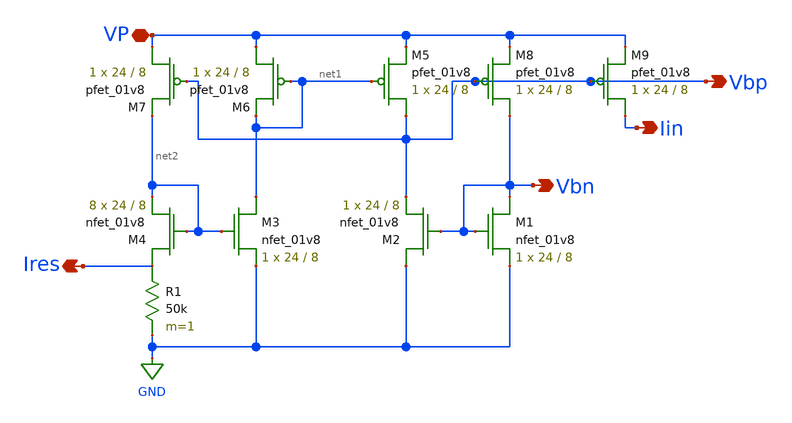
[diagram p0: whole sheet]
** sch_path: xschem/old_files/biasGen-j.sch
**.subckt biasGen-j Iin Vbp Vbn VP Ires
*.opin Iin
*.opin Vbp
*.opin Vbn
*.iopin VP
*.opin Ires
XM1 Vbn Vbn GND GND sky130_fd_pr__nfet_01v8 L=8 W=24 nf=1 ad='int((nf+1)/2) * W/nf * 0.29' as='int((nf+2)/2) * W/nf * 0.29'
+ pd='2*int((nf+1)/2) * (W/nf + 0.29)' ps='2*int((nf+2)/2) * (W/nf + 0.29)' nrd='0.29 / W' nrs='0.29 / W'
+ sa=0 sb=0 sd=0 mult=1 m=1
XM2 GND Vbn Vbp GND sky130_fd_pr__nfet_01v8 L=8 W=24 nf=1 ad='int((nf+1)/2) * W/nf * 0.29' as='int((nf+2)/2) * W/nf * 0.29'
+ pd='2*int((nf+1)/2) * (W/nf + 0.29)' ps='2*int((nf+2)/2) * (W/nf + 0.29)' nrd='0.29 / W' nrs='0.29 / W'
+ sa=0 sb=0 sd=0 mult=1 m=1
XM3 net1 net2 GND GND sky130_fd_pr__nfet_01v8 L=8 W=24 nf=1 ad='int((nf+1)/2) * W/nf * 0.29' as='int((nf+2)/2) * W/nf * 0.29'
+ pd='2*int((nf+1)/2) * (W/nf + 0.29)' ps='2*int((nf+2)/2) * (W/nf + 0.29)' nrd='0.29 / W' nrs='0.29 / W'
+ sa=0 sb=0 sd=0 mult=1 m=1
XM4 Ires net2 net2 GND sky130_fd_pr__nfet_01v8 L=8 W=24 nf=1 ad='int((nf+1)/2) * W/nf * 0.29' as='int((nf+2)/2) * W/nf * 0.29'
+ pd='2*int((nf+1)/2) * (W/nf + 0.29)' ps='2*int((nf+2)/2) * (W/nf + 0.29)' nrd='0.29 / W' nrs='0.29 / W'
+ sa=0 sb=0 sd=0 mult=8 m=8
XM5 Vbp net1 VP VDD sky130_fd_pr__pfet_01v8 L=8 W=24 nf=1 ad='int((nf+1)/2) * W/nf * 0.29' as='int((nf+2)/2) * W/nf * 0.29'
+ pd='2*int((nf+1)/2) * (W/nf + 0.29)' ps='2*int((nf+2)/2) * (W/nf + 0.29)' nrd='0.29 / W' nrs='0.29 / W'
+ sa=0 sb=0 sd=0 mult=1 m=1
XM6 VP net1 net1 VDD sky130_fd_pr__pfet_01v8 L=8 W=24 nf=1 ad='int((nf+1)/2) * W/nf * 0.29' as='int((nf+2)/2) * W/nf * 0.29'
+ pd='2*int((nf+1)/2) * (W/nf + 0.29)' ps='2*int((nf+2)/2) * (W/nf + 0.29)' nrd='0.29 / W' nrs='0.29 / W'
+ sa=0 sb=0 sd=0 mult=1 m=1
XM7 VP Vbp net2 VDD sky130_fd_pr__pfet_01v8 L=8 W=24 nf=1 ad='int((nf+1)/2) * W/nf * 0.29' as='int((nf+2)/2) * W/nf * 0.29'
+ pd='2*int((nf+1)/2) * (W/nf + 0.29)' ps='2*int((nf+2)/2) * (W/nf + 0.29)' nrd='0.29 / W' nrs='0.29 / W'
+ sa=0 sb=0 sd=0 mult=1 m=1
XM8 Vbn Vbp VP VDD sky130_fd_pr__pfet_01v8 L=8 W=24 nf=1 ad='int((nf+1)/2) * W/nf * 0.29' as='int((nf+2)/2) * W/nf * 0.29'
+ pd='2*int((nf+1)/2) * (W/nf + 0.29)' ps='2*int((nf+2)/2) * (W/nf + 0.29)' nrd='0.29 / W' nrs='0.29 / W'
+ sa=0 sb=0 sd=0 mult=1 m=1
R1 Ires GND 50k m=1
XM9 Iin Vbp VP VDD sky130_fd_pr__pfet_01v8 L=8 W=24 nf=1 ad='int((nf+1)/2) * W/nf * 0.29' as='int((nf+2)/2) * W/nf * 0.29'
+ pd='2*int((nf+1)/2) * (W/nf + 0.29)' ps='2*int((nf+2)/2) * (W/nf + 0.29)' nrd='0.29 / W' nrs='0.29 / W'
+ sa=0 sb=0 sd=0 mult=1 m=1
**.ends
.GLOBAL GND
.end
